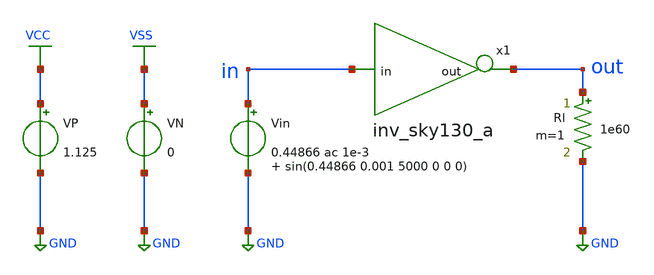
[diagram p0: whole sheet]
** sch_path: Amplifier_Inv/xschem/tb_inv_sky130_a.sch
* StefanSchippers/xschem_sky130/sky130_tests/not.sch:
* Copyright 2021 Stefan Frederik Schippers
* Licensed under the Apache License, Version 2.0 (the "License");
**.subckt tb_inv_sky130_a
VN VSS GND 0
VP VCC GND 1.125
.save i(vp)
Vin in GND 0.44866 ac 1e-3 sin(0.44866 0.001 5000 0 0 0)
.save i(vin)
Rl out GND 1e60 m=1
x1 out in inv_sky130_a
**** begin user architecture code

** opencircuitdesign pdks install
.lib $::SKYWATER_MODELS/sky130.lib.spice tt



.control

  op
  save all
  let gmn = @m.x1.x1.xm1.msky130_fd_pr__nfet_01v8[gm]
  let gmp = @m.x1.x1.xm2.msky130_fd_pr__pfet_01v8[gm]
  let gdsn = @m.x1.x1.xm1.msky130_fd_pr__nfet_01v8[gds]
  let gdsp = @m.x1.x1.xm2.msky130_fd_pr__pfet_01v8[gds]
  let cgsn = @m.x1.x1.xm1.msky130_fd_pr__nfet_01v8[cgs]
  let cgsp = @m.x1.x1.xm2.msky130_fd_pr__pfet_01v8[cgs]
  let cgdn = @m.x1.x1.xm1.msky130_fd_pr__nfet_01v8[cgd]
  let cgdp = @m.x1.x1.xm2.msky130_fd_pr__pfet_01v8[cgd]
  let vthn = @m.x1.x1.xm1.msky130_fd_pr__nfet_01v8[vth]
  write tb_inv_sky130_a_op.raw gmn gmp gdsn gdsp cgsn cgsp cgdn cgdp vthn

  ac dec 1000 1 1e6
  save all
  let gain = db(v(out)/v(in))
  let phase = phase(v(out)/v(in))
  write tb_inv_sky130_a_AC.raw gain phase

  noise v(out) Vin dec 1000 300 10k 10
  save all
  write tb_inv_sky130_a_noise.raw

  noise v(out) Vin dec 1000 300 10k
  save all
  setplot noise1
  write tb_inv_sky130_a_noise_spectrum.raw

  tran 0.1u 4m
  save all
  let pw_in = i(Vin)*v(in)
  let pw_vcc = i(Vp)*1,125
  let pw_total = pw_in+pw_vcc
  meas tran avg_pw_total AVG pw_total FROM=0 TO=2m
  meas tran avg_pw_in AVG pw_in FROM=0 TO=2m
  meas tran avg_pw_vcc AVG pw_vcc FROM=0 TO=2m
  write tb_inv_sky130_a_tran.raw v(in) v(out) avg_pw_total

  exit 0
.endc


**** end user architecture code
**.ends

* expanding   symbol:  inv_sky130_a.sym # of pins=2
** sym_path: Amplifier_Inv/xschem/inv_sky130_a.sym
** sch_path: Amplifier_Inv/xschem/inv_sky130_a.sch
.subckt inv_sky130_a out in
*.ipin in
*.opin out
x1 test net1 VCC VSS not W_N=250 L_N=1 W_P=200 L_P=0.25 m=1
XC2 out GND sky130_fd_pr__cap_mim_m3_1 W=47 L=48 MF=1 m=1
XR1 test net1 GND sky130_fd_pr__res_xhigh_po W=0.15 L=25000 mult=1 m=1
XR2 out test GND sky130_fd_pr__res_xhigh_po W=0.15 L=500 mult=1 m=1
XC1 in net1 sky130_fd_pr__cap_mim_m3_1 W=42 L=42 MF=1 m=1
.ends


* expanding   symbol:  sky130_tests/not.sym # of pins=2
** sym_path: sky130_tests/not.sym
** sch_path: sky130_tests/not.sch
.subckt not y a VCCPIN VSSPIN     W_N=1 L_N=0.15 W_P=2 L_P=0.15
*.opin y
*.ipin a
XM1 DN a VSSPIN VSSPIN sky130_fd_pr__nfet_01v8 L=L_N W=W_N nf=1 ad='int((1 + 1)/2) * W_N / 1 * 0.29'
+ as='int((1 + 2)/2) * W_N / 1 * 0.29' pd='2*int((1 + 1)/2) * (W_N / 1 + 0.29)' ps='2*int((1 + 2)/2) * (W_N / 1 + 0.29)'
+ nrd='0.29 / W_N ' nrs='0.29 / W_N ' sa=0 sb=0 sd=0 mult=1 m=1
XM2 DP a VCCPIN VCCPIN sky130_fd_pr__pfet_01v8 L=L_P W=W_P nf=1 ad='int((nf+1)/2) * W/nf * 0.29' as='int((nf+2)/2) * W/nf * 0.29'
+ pd='2*int((nf+1)/2) * (W/nf + 0.29)' ps='2*int((nf+2)/2) * (W/nf + 0.29)' nrd='0.29 / W' nrs='0.29 / W'
+ sa=0 sb=0 sd=0 mult=1 m=1
Vmeas DP y 0
.save i(vmeas)
Vmeas1 y DN 0
.save i(vmeas1)
.save v(dp)
.save v(dn)
.ends

.GLOBAL GND
.GLOBAL VSS
.GLOBAL VCC
.end
